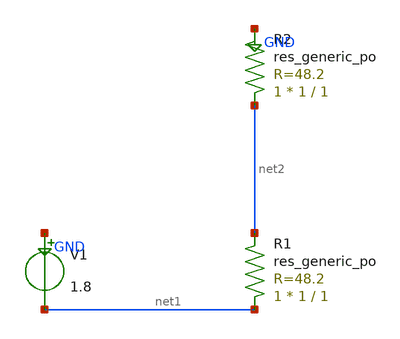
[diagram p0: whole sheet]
** sch_path: sim/pdk-smoke/testbench/tb_pdk_smoke.sch
**.subckt tb_pdk_smoke
V1 GND net1 1.8
XR1 net1 net2 sky130_fd_pr__res_generic_po W=1 L=1 m=1
XR2 net2 GND sky130_fd_pr__res_generic_po W=1 L=1 m=1
**** begin user architecture code

** sky130 PDK model include (tt corner) -- patched per-point by sim/harness
.lib $::SKYWATER_MODELS/sky130.lib.spice tt
.op

**** end user architecture code
**.ends
.GLOBAL GND
.end
